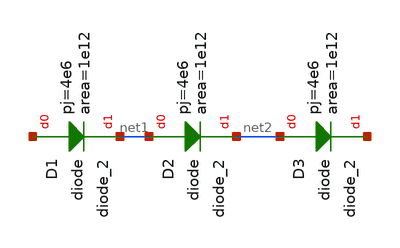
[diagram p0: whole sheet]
** sch_path: DISEÑO/ANALOGICO/V;SI/BOMBA DE CARGA/xschem/diode.sch
**.subckt diode
XD1 net3 net1 sky130_fd_pr__diode_2 area=1e12 pj=4e6
XD2 net1 net2 sky130_fd_pr__diode_2 area=1e12 pj=4e6
XD3 net2 net4 sky130_fd_pr__diode_2 area=1e12 pj=4e6
**.ends
.end
